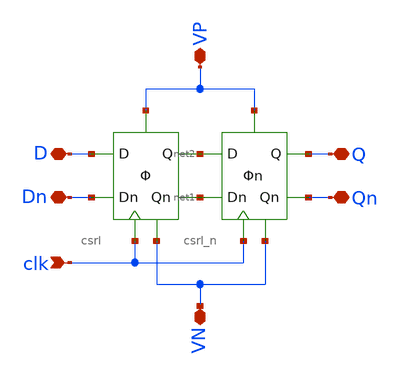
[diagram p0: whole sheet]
** sch_path: lib/digital/schematic/csrl_falling_edge.sch
**.subckt csrl_falling_edge clk D Dn Q Qn VP VN
*.ipin clk
*.iopin D
*.iopin Dn
*.iopin Q
*.iopin Qn
*.iopin VP
*.iopin VN
X1 D Dn net1 net2 VN clk VP csrl
X2 net2 net1 Qn Q VN clk VP csrl_n
**.ends
.end
